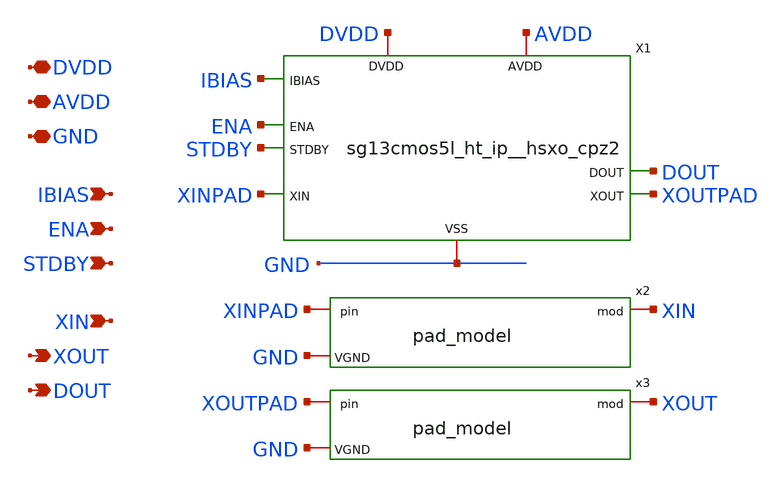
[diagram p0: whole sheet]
** sch_path: xschem/dut_with_package.sch
**.subckt dut_with_package DVDD GND AVDD ENA STDBY XIN XOUT DOUT IBIAS
*.iopin DVDD
*.iopin GND
*.iopin AVDD
*.ipin ENA
*.ipin STDBY
*.ipin XIN
*.opin XOUT
*.opin DOUT
*.ipin IBIAS
X1 XOUTPAD XINPAD ENA STDBY DOUT AVDD DVDD GND IBIAS sg13cmos5l_ht_ip__hsxo_cpz2
x3 GND XOUTPAD XOUT pad_model
x2 GND XINPAD XIN pad_model
**.ends
.end
